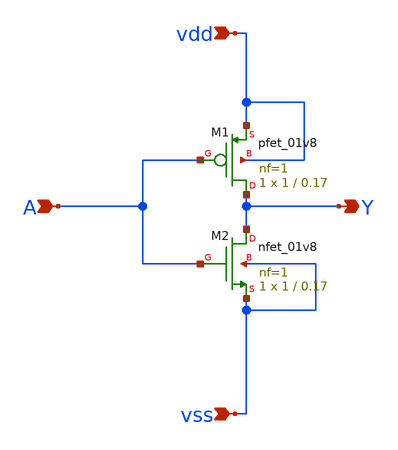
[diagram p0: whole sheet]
** sch_path: xschem/inv_x1/inv_x1.sch
**.subckt inv_x1 vdd vss Y A
*.ipin vdd
*.ipin vss
*.opin Y
*.ipin A
XM2 Y A vss vss sky130_fd_pr__nfet_01v8 L=0.17 W=1 nf=1 ad={int((nf+1)/2) * W/nf * 0.29} as={int((nf+2)/2) * W/nf * 0.29}
+ pd={2*int((nf+1)/2) * (W/nf + 0.29)} ps={2*int((nf+2)/2) * (W/nf + 0.29)} nrd={0.29 / W} nrs={0.29 / W}
+ sa=0 sb=0 sd=0 mult=1 m=1
XM1 Y A vdd vdd sky130_fd_pr__pfet_01v8 L=0.17 W=1 nf=1 ad={int((nf+1)/2) * W/nf * 0.29} as={int((nf+2)/2) * W/nf * 0.29}
+ pd={2*int((nf+1)/2) * (W/nf + 0.29)} ps={2*int((nf+2)/2) * (W/nf + 0.29)} nrd={0.29 / W} nrs={0.29 / W}
+ sa=0 sb=0 sd=0 mult=1 m=1
**.ends
.end
